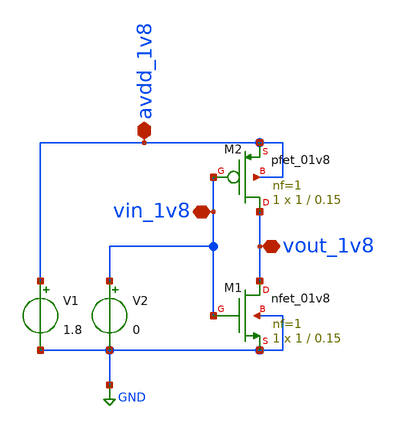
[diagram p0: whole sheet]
** sch_path: ISSCC25/submitted_notebooks/current_mirror_ota_optimization/characterization/sky130/xschem_cds/schematics/test_inverter.sch
**.subckt test_inverter avdd_1v8 vin_1v8 vout_1v8
*.iopin avdd_1v8
*.iopin vin_1v8
*.iopin vout_1v8
V1 avdd_1v8 GND 1.8
XM1 vout_1v8 vin_1v8 GND GND sky130_fd_pr__nfet_01v8 L=0.15 W=1 nf=1 ad='int((nf+1)/2) * W/nf * 0.29'
+ as='int((nf+2)/2) * W/nf * 0.29' pd='2*int((nf+1)/2) * (W/nf + 0.29)' ps='2*int((nf+2)/2) * (W/nf + 0.29)'
+ nrd='0.29 / W' nrs='0.29 / W' sa=0 sb=0 sd=0 mult=1 m=1
XM2 vout_1v8 vin_1v8 avdd_1v8 avdd_1v8 sky130_fd_pr__pfet_01v8 L=0.15 W=1 nf=1 ad='int((nf+1)/2) * W/nf * 0.29'
+ as='int((nf+2)/2) * W/nf * 0.29' pd='2*int((nf+1)/2) * (W/nf + 0.29)' ps='2*int((nf+2)/2) * (W/nf + 0.29)'
+ nrd='0.29 / W' nrs='0.29 / W' sa=0 sb=0 sd=0 mult=1 m=1
V2 vin_1v8 GND 0
**** begin user architecture code



.lib /opt/pdk/open_pdks/sky130/sky130A/libs.tech/ngspice/sky130.lib.spice tt

.control
	dc V2 0 1.8 0.01
	plot v(vout_1v8)
.endc

.save all



**** end user architecture code
**.ends
.GLOBAL GND
.end
